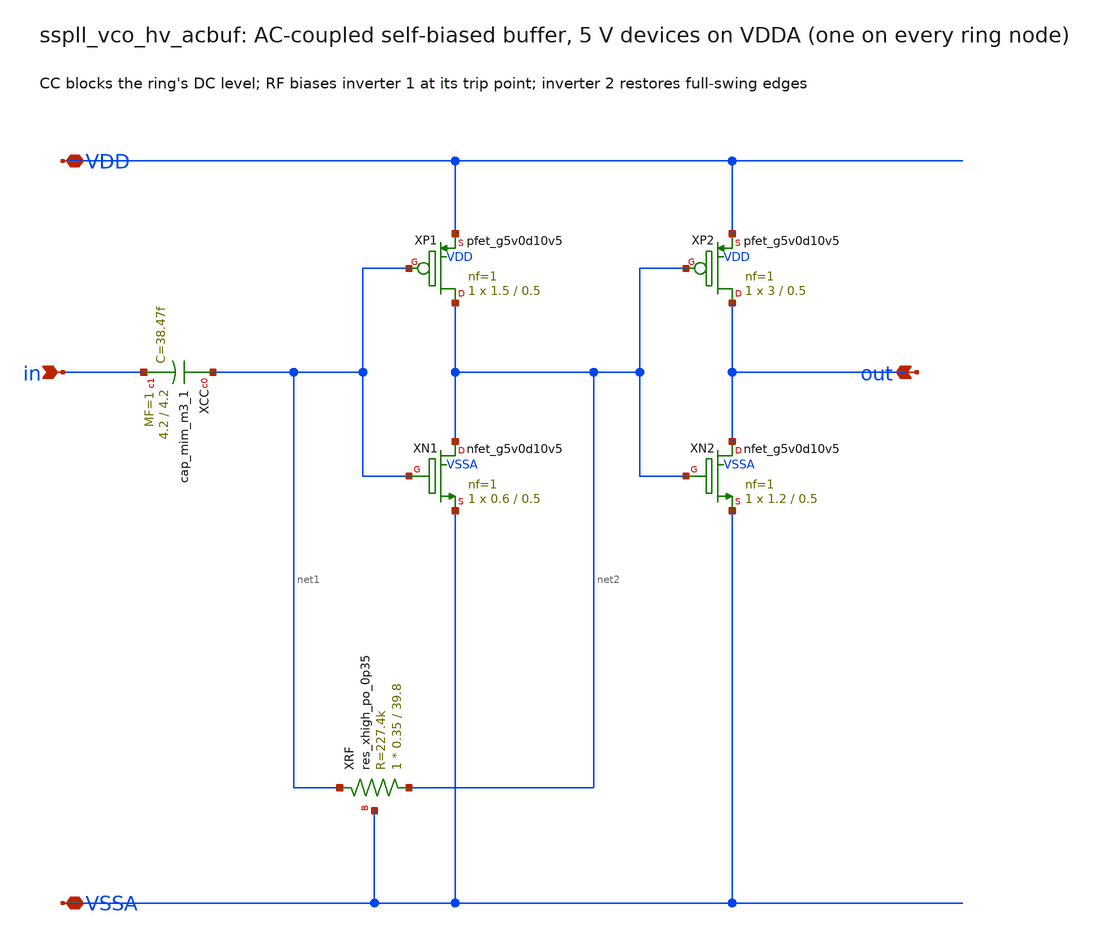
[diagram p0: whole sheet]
** sch_path: xschem/vco_hv/sspll_vco_hv_acbuf.sch
**.subckt sspll_vco_hv_acbuf VDD VSSA in out
*.iopin VDD
*.iopin VSSA
*.ipin in
*.opin out
XXCC net1 in sky130_fd_pr__cap_mim_m3_1 W=4.2 L=4.2 MF=1 m=1
XXP1 net2 net1 VDD VDD sky130_fd_pr__pfet_g5v0d10v5 L=0.5 W=1.5 nf=1 ad='int((nf+1)/2) * W/nf * 0.29'
+ as='int((nf+2)/2) * W/nf * 0.29' pd='2*int((nf+1)/2) * (W/nf + 0.29)' ps='2*int((nf+2)/2) * (W/nf + 0.29)'
+ nrd='0.29 / W' nrs='0.29 / W' sa=0 sb=0 sd=0 mult=1 m=1
XXN1 net2 net1 VSSA VSSA sky130_fd_pr__nfet_g5v0d10v5 L=0.5 W=0.6 nf=1 ad='int((nf+1)/2) * W/nf * 0.29'
+ as='int((nf+2)/2) * W/nf * 0.29' pd='2*int((nf+1)/2) * (W/nf + 0.29)' ps='2*int((nf+2)/2) * (W/nf + 0.29)'
+ nrd='0.29 / W' nrs='0.29 / W' sa=0 sb=0 sd=0 mult=1 m=1
XXRF net2 net1 VSSA sky130_fd_pr__res_xhigh_po_0p35 L=39.8 mult=1 m=1
XXP2 out net2 VDD VDD sky130_fd_pr__pfet_g5v0d10v5 L=0.5 W=3 nf=1 ad='int((nf+1)/2) * W/nf * 0.29' as='int((nf+2)/2) * W/nf * 0.29'
+ pd='2*int((nf+1)/2) * (W/nf + 0.29)' ps='2*int((nf+2)/2) * (W/nf + 0.29)' nrd='0.29 / W' nrs='0.29 / W'
+ sa=0 sb=0 sd=0 mult=1 m=1
XXN2 out net2 VSSA VSSA sky130_fd_pr__nfet_g5v0d10v5 L=0.5 W=1.2 nf=1 ad='int((nf+1)/2) * W/nf * 0.29'
+ as='int((nf+2)/2) * W/nf * 0.29' pd='2*int((nf+1)/2) * (W/nf + 0.29)' ps='2*int((nf+2)/2) * (W/nf + 0.29)'
+ nrd='0.29 / W' nrs='0.29 / W' sa=0 sb=0 sd=0 mult=1 m=1
**.ends
.end
